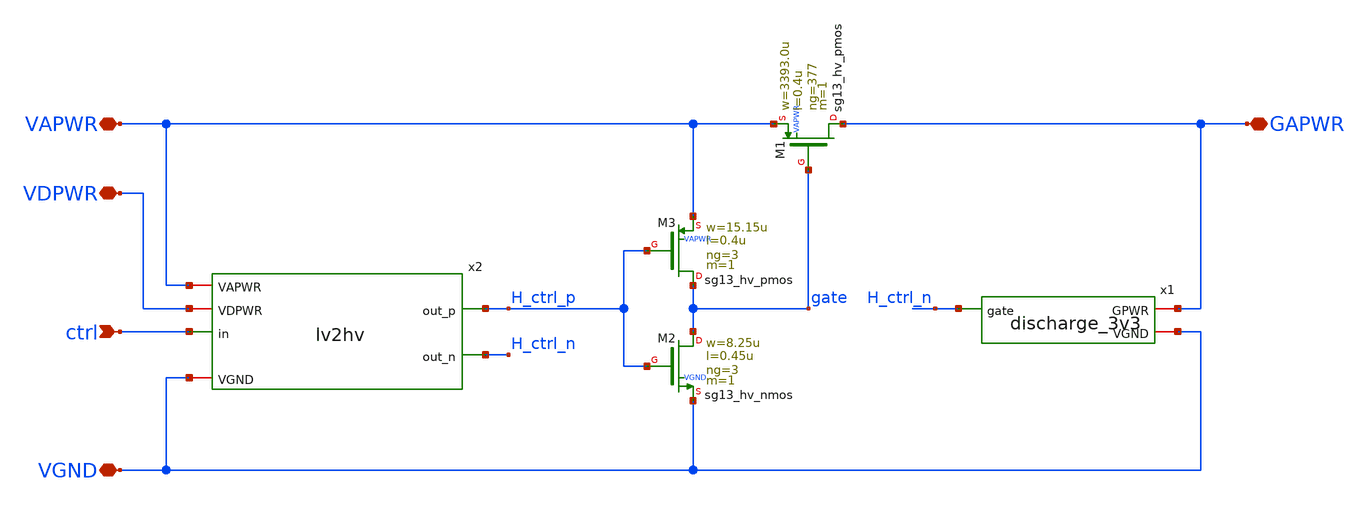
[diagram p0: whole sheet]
** sch_path: pg/ihp-sg13cmos5l/tt_pg_3v3_2/xschem/tt_pg_3v3_2.sch
**.subckt tt_pg_3v3_2 ctrl VDPWR VGND GAPWR VAPWR
*.ipin ctrl
*.iopin VDPWR
*.iopin VGND
*.iopin GAPWR
*.iopin VAPWR
x1 VGND GAPWR H_ctrl_n discharge_3v3
x2 VGND VDPWR VAPWR ctrl H_ctrl_p H_ctrl_n lv2hv
XM1 GAPWR gate VAPWR VAPWR sg13_hv_pmos w=3393.0u l=0.4u ng=377 m=1
XM2 gate H_ctrl_p VGND VGND sg13_hv_nmos w=8.25u l=0.45u ng=3 m=1
XM3 gate H_ctrl_p VAPWR VAPWR sg13_hv_pmos w=15.15u l=0.4u ng=3 m=1
**.ends
.end
